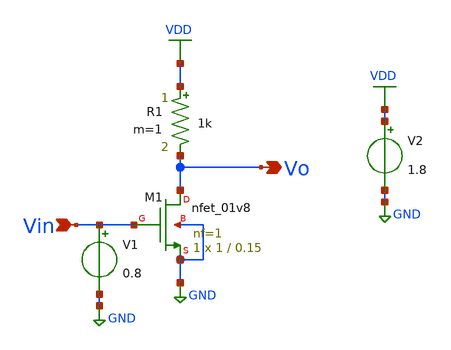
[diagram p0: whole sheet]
** sch_path: SINGLE_STAGE_AMP/CS_RES/cs_res_parametric.sch
**.subckt cs_res_parametric Vin Vo
*.ipin Vin
*.opin Vo
R1 VDD Vo 1k m=1
V1 Vin GND 0.8
V2 VDD GND 1.8
XM1 Vo Vin GND GND sky130_fd_pr__nfet_01v8 L=0.15 W=1 nf=1 ad='int((nf+1)/2) * W/nf * 0.29' as='int((nf+2)/2) * W/nf * 0.29'
+ pd='2*int((nf+1)/2) * (W/nf + 0.29)' ps='2*int((nf+2)/2) * (W/nf + 0.29)' nrd='0.29 / W' nrs='0.29 / W'
+ sa=0 sb=0 sd=0 mult=1 m=1
**** begin user architecture code


.option scale=1u
.lib /home/varun/.ciel/ciel/sky130/versions/1689ac3f2dc763876eaf967227c7dfe831b031ae/sky130A/libs.tech/ngspice/sky130.lib.spice tt

.control
  save all

  * Sweep R1 from 1k to 9k with 2k step size (1k, 3k, 5k, 7k, 9k)
  foreach r_val 1k 3k 5k 7k 9k
    alter R1 $r_val
    dc V1 0 1.8 0.01
  end

  * Graph 1: Vout vs Vin across all 5 resistor steps
  plot dc1.v(Vo) dc2.v(Vo) dc3.v(Vo) dc4.v(Vo) dc5.v(Vo) title 'Vout vs Vin (R1 = 1k, 3k, 5k, 7k, 9k)'

  * Graph 2: Voltage Gain d(Vout)/d(Vin) vs Vin
  plot deriv(dc1.v(Vo)) deriv(dc2.v(Vo)) deriv(dc3.v(Vo)) deriv(dc4.v(Vo)) deriv(dc5.v(Vo)) title 'Small-Signal Gain Av = d(Vo)/d(Vin)'
.endc


**** end user architecture code
**.ends
.GLOBAL VDD
.GLOBAL GND
.end
